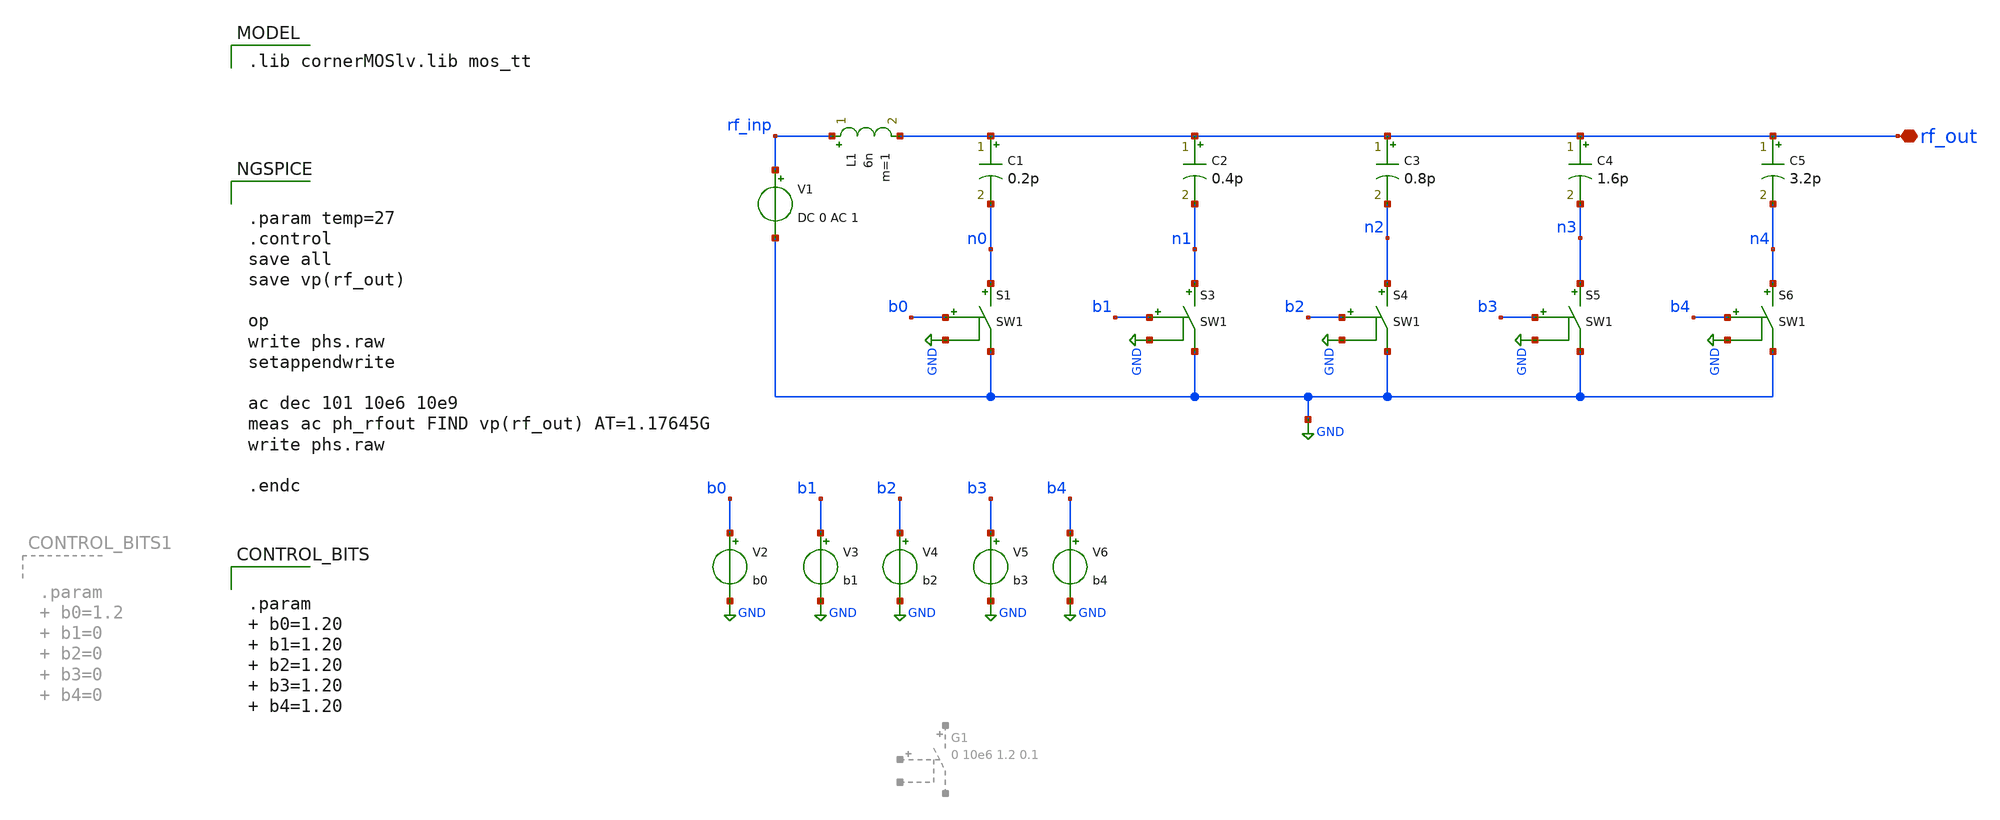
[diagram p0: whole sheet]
** sch_path: xschem/phs.sch
**.subckt phs rf_out
*.iopin rf_out
L1 rf_inp rf_out 6n m=1
C1 rf_out n0 0.2p m=1
C2 rf_out n1 0.4p m=1
C3 rf_out n2 0.8p m=1
C4 rf_out n3 1.6p m=1
C5 rf_out n4 3.2p m=1
V1 rf_inp GND DC 0 AC 1
V2 b0 GND b0
V3 b1 GND b1
V4 b2 GND b2
V5 b3 GND b3
V6 b4 GND b4
S3 n1 GND b1 GND SW1
S4 n2 GND b2 GND SW1
S5 n3 GND b3 GND SW1
S6 n4 GND b4 GND SW1
S1 n0 GND b0 GND SW1
**** begin user architecture code
 .lib cornerMOSlv.lib mos_tt



.param temp=27
.control
save all
save vp(rf_out)

op
write phs.raw
setappendwrite

ac dec 101 10e6 10e9
meas ac ph_rfout FIND vp(rf_out) AT=1.17645G
write phs.raw

.endc




.param   b0=1.20  b1=1.20  b2=1.20  b3=1.20  b4=1.20


**** end user architecture code
**.ends
.GLOBAL GND
**** begin user architecture code
.MODEL SW1 SW   VT=0.9 VH=0.01  RON=0.01 ROFF=10G
**** end user architecture code
.end
